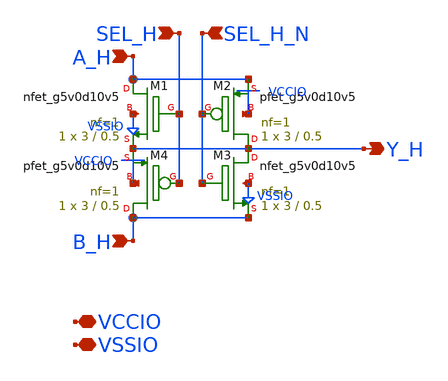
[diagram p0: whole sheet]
** sch_path: gpiov2_octl_mux.sch
* Copyright 2023 David Mitchell Bailey
* Licensed under the Apache License, Version 2.0 (the "License");
* you may not use this file except in compliance with the License.
* You may obtain a copy of the License at
* https://www.apache.org/licenses/LICENSE-2.0
* Unless required by applicable law or agreed to in writing, software
* distributed under the License is distributed on an "AS IS" BASIS,
* WITHOUT WARRANTIES OR CONDITIONS OF ANY KIND, either express or implied.
* See the License for the specific language governing permissions and
* limitations under the License.
**.subckt gpiov2_octl_mux A_H VCCIO VSSIO Y_H B_H SEL_H SEL_H_N
*.ipin A_H
*.iopin VCCIO
*.iopin VSSIO
*.opin Y_H
*.ipin B_H
*.ipin SEL_H
*.ipin SEL_H_N
XM1 A_H SEL_H Y_H VSSIO sky130_fd_pr__nfet_g5v0d10v5 L=0.5 W=3 nf=1 ad='int((nf+1)/2) * W/nf * 0.29'
+ as='int((nf+2)/2) * W/nf * 0.29' pd='2*int((nf+1)/2) * (W/nf + 0.29)' ps='2*int((nf+2)/2) * (W/nf + 0.29)'
+ nrd='0.29 / W' nrs='0.29 / W' sa=0 sb=0 sd=0 mult=1 m=1
XM2 Y_H SEL_H_N A_H VCCIO sky130_fd_pr__pfet_g5v0d10v5 L=0.5 W=3 nf=1 ad='int((nf+1)/2) * W/nf * 0.29'
+ as='int((nf+2)/2) * W/nf * 0.29' pd='2*int((nf+1)/2) * (W/nf + 0.29)' ps='2*int((nf+2)/2) * (W/nf + 0.29)'
+ nrd='0.29 / W' nrs='0.29 / W' sa=0 sb=0 sd=0 mult=1 m=1
XM3 Y_H SEL_H_N B_H VSSIO sky130_fd_pr__nfet_g5v0d10v5 L=0.5 W=3 nf=1 ad='int((nf+1)/2) * W/nf * 0.29'
+ as='int((nf+2)/2) * W/nf * 0.29' pd='2*int((nf+1)/2) * (W/nf + 0.29)' ps='2*int((nf+2)/2) * (W/nf + 0.29)'
+ nrd='0.29 / W' nrs='0.29 / W' sa=0 sb=0 sd=0 mult=1 m=1
XM4 B_H SEL_H Y_H VCCIO sky130_fd_pr__pfet_g5v0d10v5 L=0.5 W=3 nf=1 ad='int((nf+1)/2) * W/nf * 0.29'
+ as='int((nf+2)/2) * W/nf * 0.29' pd='2*int((nf+1)/2) * (W/nf + 0.29)' ps='2*int((nf+2)/2) * (W/nf + 0.29)'
+ nrd='0.29 / W' nrs='0.29 / W' sa=0 sb=0 sd=0 mult=1 m=1
**.ends
.end
